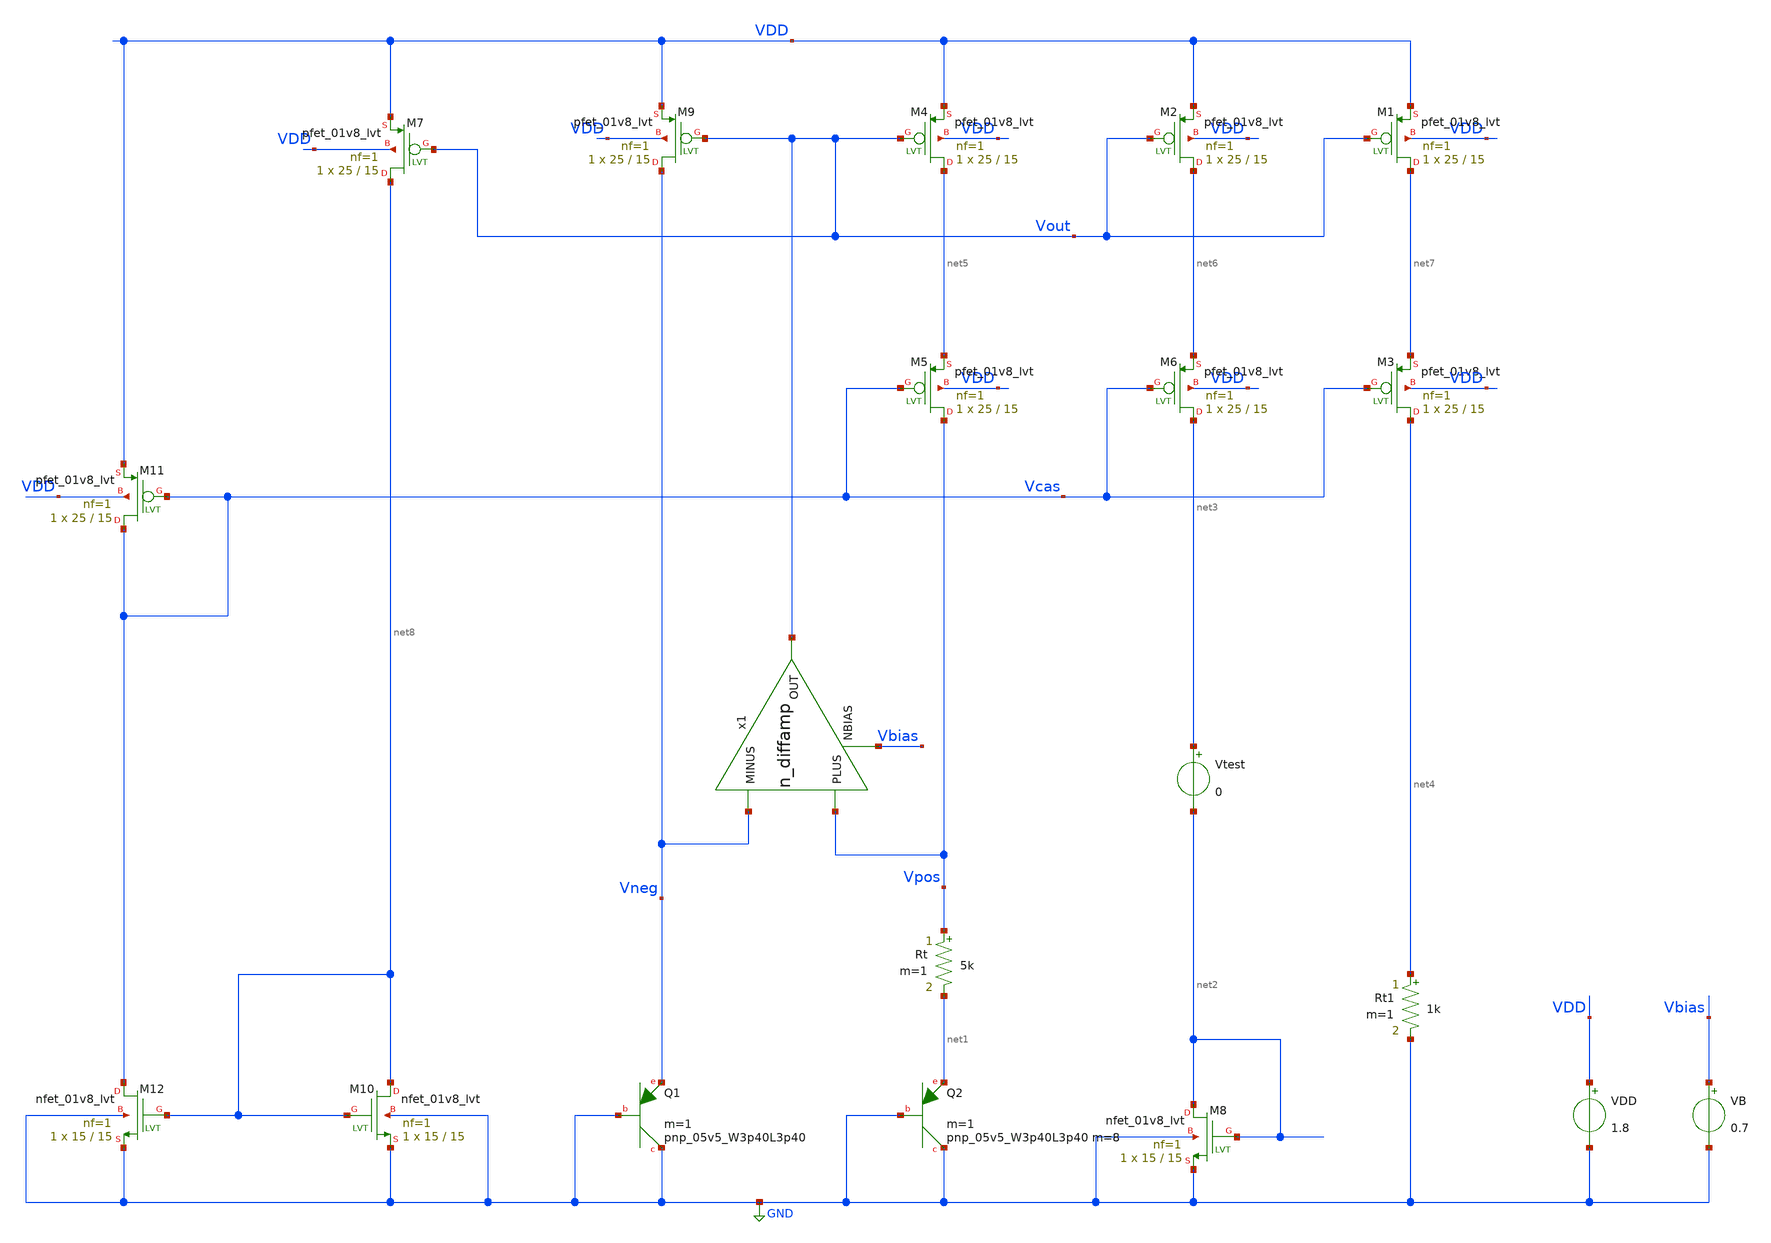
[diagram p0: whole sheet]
** sch_path: design/bgr_new/BGR.sch
* Copyright 2021 Stefan Frederik Schippers
* Licensed under the Apache License, Version 2.0 (the "License");
* you may not use this file except in compliance with the License.
* You may obtain a copy of the License at
* https://www.apache.org/licenses/LICENSE-2.0
* Unless required by applicable law or agreed to in writing, software
* distributed under the License is distributed on an "AS IS" BASIS,
* WITHOUT WARRANTIES OR CONDITIONS OF ANY KIND, either express or implied.
* See the License for the specific language governing permissions and
* limitations under the License.
**.subckt BGR
XQ1 GND GND Vneg sky130_fd_pr__pnp_05v5_W3p40L3p40 m=1
XQ2 GND GND net1 sky130_fd_pr__pnp_05v5_W3p40L3p40 m=8 m=1
XM8 net2 net2 GND GND sky130_fd_pr__nfet_01v8_lvt L=15 W=15 nf=1 ad='int((nf+1)/2) * W/nf * 0.29' as='int((nf+2)/2) * W/nf * 0.29'
+ pd='2*int((nf+1)/2) * (W/nf + 0.29)' ps='2*int((nf+2)/2) * (W/nf + 0.29)' nrd='0.29 / W' nrs='0.29 / W'
+ sa=0 sb=0 sd=0 mult=1 m=1
Vtest net3 net2 0
Rt1 net4 GND 1k m=1
Rt Vpos net1 5k m=1
VDD VDD GND 1.8
x1 Vout Vneg Vpos Vbias n_diffamp
VB Vbias GND 0.7
XM3 net4 Vcas net7 VDD sky130_fd_pr__pfet_01v8_lvt L=15 W=25 nf=1 ad='int((nf+1)/2) * W * 0.29' as='int((nf+2)/2) * W * 0.29'
+ pd='2*int((nf+1)/2) * (W + 0.29)' ps='2*int((nf+2)/2) * (W + 0.29)' nrd='0.29 / W / nf' nrs='0.29 / W / nf'
+ sa=0 sb=0 sd=0 mult=1 m=1
XM10 net8 net8 GND GND sky130_fd_pr__nfet_01v8_lvt L=15 W=15 nf=1 ad='int((nf+1)/2) * W/nf * 0.29' as='int((nf+2)/2) * W/nf * 0.29'
+ pd='2*int((nf+1)/2) * (W/nf + 0.29)' ps='2*int((nf+2)/2) * (W/nf + 0.29)' nrd='0.29 / W' nrs='0.29 / W'
+ sa=0 sb=0 sd=0 mult=1 m=1
XM12 Vcas net8 GND GND sky130_fd_pr__nfet_01v8_lvt L=15 W=15 nf=1 ad='int((nf+1)/2) * W/nf * 0.29' as='int((nf+2)/2) * W/nf * 0.29'
+ pd='2*int((nf+1)/2) * (W/nf + 0.29)' ps='2*int((nf+2)/2) * (W/nf + 0.29)' nrd='0.29 / W' nrs='0.29 / W'
+ sa=0 sb=0 sd=0 mult=1 m=1
XM1 net7 Vout VDD VDD sky130_fd_pr__pfet_01v8_lvt L=15 W=25 nf=1 ad='int((nf+1)/2) * W * 0.29' as='int((nf+2)/2) * W * 0.29'
+ pd='2*int((nf+1)/2) * (W + 0.29)' ps='2*int((nf+2)/2) * (W + 0.29)' nrd='0.29 / W / nf' nrs='0.29 / W / nf'
+ sa=0 sb=0 sd=0 mult=1 m=1
XM2 net6 Vout VDD VDD sky130_fd_pr__pfet_01v8_lvt L=15 W=25 nf=1 ad='int((nf+1)/2) * W * 0.29' as='int((nf+2)/2) * W * 0.29'
+ pd='2*int((nf+1)/2) * (W + 0.29)' ps='2*int((nf+2)/2) * (W + 0.29)' nrd='0.29 / W / nf' nrs='0.29 / W / nf'
+ sa=0 sb=0 sd=0 mult=1 m=1
XM4 net5 Vout VDD VDD sky130_fd_pr__pfet_01v8_lvt L=15 W=25 nf=1 ad='int((nf+1)/2) * W * 0.29' as='int((nf+2)/2) * W * 0.29'
+ pd='2*int((nf+1)/2) * (W + 0.29)' ps='2*int((nf+2)/2) * (W + 0.29)' nrd='0.29 / W / nf' nrs='0.29 / W / nf'
+ sa=0 sb=0 sd=0 mult=1 m=1
XM5 Vpos Vcas net5 VDD sky130_fd_pr__pfet_01v8_lvt L=15 W=25 nf=1 ad='int((nf+1)/2) * W * 0.29' as='int((nf+2)/2) * W * 0.29'
+ pd='2*int((nf+1)/2) * (W + 0.29)' ps='2*int((nf+2)/2) * (W + 0.29)' nrd='0.29 / W / nf' nrs='0.29 / W / nf'
+ sa=0 sb=0 sd=0 mult=1 m=1
XM6 net3 Vcas net6 VDD sky130_fd_pr__pfet_01v8_lvt L=15 W=25 nf=1 ad='int((nf+1)/2) * W * 0.29' as='int((nf+2)/2) * W * 0.29'
+ pd='2*int((nf+1)/2) * (W + 0.29)' ps='2*int((nf+2)/2) * (W + 0.29)' nrd='0.29 / W / nf' nrs='0.29 / W / nf'
+ sa=0 sb=0 sd=0 mult=1 m=1
XM7 net8 Vout VDD VDD sky130_fd_pr__pfet_01v8_lvt L=15 W=25 nf=1 ad='int((nf+1)/2) * W * 0.29' as='int((nf+2)/2) * W * 0.29'
+ pd='2*int((nf+1)/2) * (W + 0.29)' ps='2*int((nf+2)/2) * (W + 0.29)' nrd='0.29 / W / nf' nrs='0.29 / W / nf'
+ sa=0 sb=0 sd=0 mult=1 m=1
XM9 Vneg Vout VDD VDD sky130_fd_pr__pfet_01v8_lvt L=15 W=25 nf=1 ad='int((nf+1)/2) * W * 0.29' as='int((nf+2)/2) * W * 0.29'
+ pd='2*int((nf+1)/2) * (W + 0.29)' ps='2*int((nf+2)/2) * (W + 0.29)' nrd='0.29 / W / nf' nrs='0.29 / W / nf'
+ sa=0 sb=0 sd=0 mult=1 m=1
XM11 Vcas Vcas VDD VDD sky130_fd_pr__pfet_01v8_lvt L=15 W=25 nf=1 ad='int((nf+1)/2) * W * 0.29' as='int((nf+2)/2) * W * 0.29'
+ pd='2*int((nf+1)/2) * (W + 0.29)' ps='2*int((nf+2)/2) * (W + 0.29)' nrd='0.29 / W / nf' nrs='0.29 / W / nf'
+ sa=0 sb=0 sd=0 mult=1 m=1
**** begin user architecture code

** opencircuitdesign pdks install
.lib $::SKYWATER_MODELS/sky130.lib.spice tt_mm




.options savecurrents

*** plot vbgp with variation in supply voltage
*Vdd VDD GND 3.3
*V_en en GND 3.3
*.dc Vdd 2 4 0.1
*.control
*run
*print Vbgp
*plot V(Vbgp)
*.endc

*** plot vbgp with variation in temperature @3.3V
*Vdd VDD GND 3.3
*V_en en GND 3.3
*.dc temp -40 100 1 Rt 4k 6k 1k
.dc temp -40 100 1

.control
run
*print V(VE)
*plot V(VE)
*plot deriv(V(VE))/1.202344
plot V(Vout) V(Vcas) V(Vpos) V(Vneg)
plot deriv(V(Vout))/1.202344
.endc

*** plot voltage coefficient
*Vdd VDD GND 3.3
*V_en en GND 3.3
*.dc Vdd 2 4 0.1
*.control
*run
*plot deriv(V(Vbgp))
*.endc

*** plot temperature coefficient
*Vdd VDD GND 3.3
*V_en en GND 3.3
*.dc temp -40 140 1
*.control
*run
*plot deriv(V(Vbgp))/1.202344
*.endc



*** enable pin
*Vdd VDD GND 3.3
*V_en en GND PULSE(0 3.3 0 200us 200us 600us 2000us 0)
*.tran 1u 2000us
*.control
*run
*plot V(en)
*plot -I(VDD)
*.endc


**** end user architecture code
**.ends

* expanding   symbol:  sky130_tests/n_diffamp.sym # of pins=4
** sym_path: sky130_tests/n_diffamp.sym
** sch_path: sky130_tests/n_diffamp.sch
.subckt n_diffamp OUT MINUS PLUS NBIAS
*.ipin PLUS
*.ipin MINUS
*.opin OUT
*.ipin NBIAS
XM1 net1 PLUS S GND sky130_fd_pr__nfet_01v8_lvt L=0.3 W=2 nf=1 ad='int((1 + 1)/2) * 2 / 1 * 0.29' as='int((1 + 2)/2) * 2 / 1 * 0.29'
+ pd='2*int((1 + 1)/2) * (2 / 1 + 0.29)' ps='2*int((1 + 2)/2) * (2 / 1 + 0.29)' nrd='0.29 / 2 ' nrs='0.29 / 2 '
+ sa=0 sb=0 sd=0 mult=1 m=1
XM2 OUT MINUS S GND sky130_fd_pr__nfet_01v8_lvt L=0.3 W=2 nf=1 ad='int((1 + 1)/2) * 2 / 1 * 0.29' as='int((1 + 2)/2) * 2 / 1 * 0.29'
+ pd='2*int((1 + 1)/2) * (2 / 1 + 0.29)' ps='2*int((1 + 2)/2) * (2 / 1 + 0.29)' nrd='0.29 / 2 ' nrs='0.29 / 2 '
+ sa=0 sb=0 sd=0 mult=1 m=1
XM3 OUT net1 VDD VDD sky130_fd_pr__pfet_01v8_lvt L=0.8 W=4 nf=1 ad='int((1 + 1)/2) * 4 / 1 * 0.29' as='int((1 + 2)/2) * 4 / 1 * 0.29'
+ pd='2*int((1 + 1)/2) * (4 / 1 + 0.29)' ps='2*int((1 + 2)/2) * (4 / 1 + 0.29)' nrd='0.29 / 4 ' nrs='0.29 / 4 '
+ sa=0 sb=0 sd=0 mult=1 m=1
XM4 net1 net1 VDD VDD sky130_fd_pr__pfet_01v8_lvt L=0.8 W=4 nf=1 ad='int((1 + 1)/2) * 4 / 1 * 0.29' as='int((1 + 2)/2) * 4 / 1 * 0.29'
+ pd='2*int((1 + 1)/2) * (4 / 1 + 0.29)' ps='2*int((1 + 2)/2) * (4 / 1 + 0.29)' nrd='0.29 / 4 ' nrs='0.29 / 4 '
+ sa=0 sb=0 sd=0 mult=1 m=1
XM5 net2 NBIAS GND GND sky130_fd_pr__nfet_01v8 L=2 W=0.7 nf=1 ad='int((nf+1)/2) * W/nf * 0.29' as='int((nf+2)/2) * W/nf * 0.29'
+ pd='2*int((nf+1)/2) * (W/nf + 0.29)' ps='2*int((nf+2)/2) * (W/nf + 0.29)' nrd='0.29 / W' nrs='0.29 / W'
+ sa=0 sb=0 sd=0 mult=1 m=1
XR1 GND S GND sky130_fd_pr__res_xhigh_po_0p35 L=50 mult=1 m=1
V5 S net2 0
.save i(v5)
.ends

.GLOBAL GND
.GLOBAL VDD
.end
